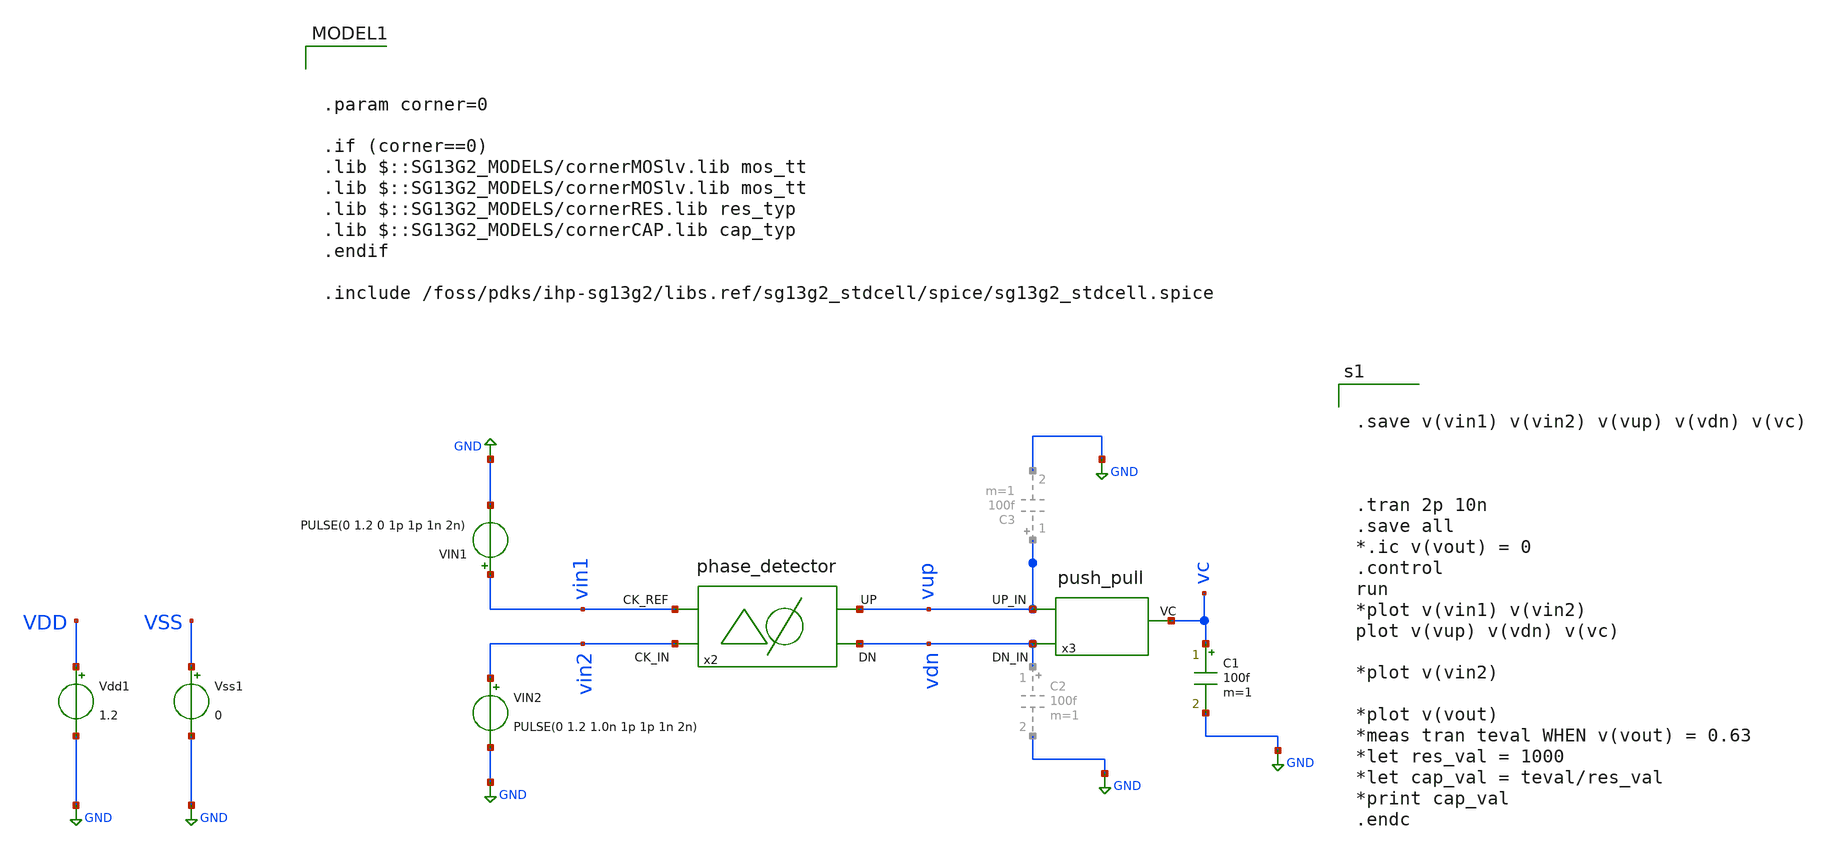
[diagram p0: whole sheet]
** sch_path: xschem/phase_detector/tb_QPD.sch
**.subckt tb_QPD
VIN1 vin1 GND PULSE(0 1.2 0 1p 1p 1n 2n)
x2 vin2 vup vin1 vdn phase_detector
VIN2 vin2 GND PULSE(0 1.2 1.0n 1p 1p 1n 2n)
x3 vup vc vdn push_pull
C1 vc GND 100f m=1
Vss1 VSS GND 0
Vdd1 VDD GND 1.2
**** begin user architecture code


.save v(vin1) v(vin2) v(vup) v(vdn) v(vc)



.tran 2p 10n
.save all
*.ic v(vout) = 0
.control
run
*plot v(vin1) v(vin2)
plot v(vup) v(vdn) v(vc)

*plot v(vin2)

*plot v(vout)
*meas tran teval WHEN v(vout) = 0.63
*let res_val = 1000
*let cap_val = teval/res_val
*print cap_val
.endc




.param corner=0

.if (corner==0)
.lib $::SG13G2_MODELS/cornerMOSlv.lib mos_tt
.lib $::SG13G2_MODELS/cornerMOSlv.lib mos_tt
.lib $::SG13G2_MODELS/cornerRES.lib res_typ
.lib $::SG13G2_MODELS/cornerCAP.lib cap_typ
.endif

.include /foss/pdks/ihp-sg13g2/libs.ref/sg13g2_stdcell/spice/sg13g2_stdcell.spice

**** end user architecture code
**.ends

* expanding   symbol:  /foss/designs/DLL/phase_detector.sym # of pins=4
** sym_path: xschem/phase_detector/phase_detector.sym
** sch_path: xschem/phase_detector/phase_detector.sch
.subckt phase_detector CK_IN UP CK_REF DN
*.opin UP
*.ipin CK_IN
*.ipin CK_REF
*.opin DN
XM7 net2 CK_IN VDD VDD sg13_lv_pmos w=5u l=4u ng=1 m=1 mm_ok=1
XM8 net1 CK_IN VDD VDD sg13_lv_pmos w=5u l=4u ng=1 m=1 mm_ok=1
XM9 net2 CK_REF net1 net1 sg13_lv_nmos w=2u l=5u ng=5 m=1 mm_ok=1
XM10 net2 DN net1 VSS sg13_lv_nmos w=2u l=5u ng=5 m=1 mm_ok=1
XM11 net1 CK_IN VSS VSS sg13_lv_nmos w=2u l=5u ng=5 m=1 mm_ok=1
XM6 UP net2 VDD VDD sg13_lv_pmos w=5u l=4u ng=1 m=1 mm_ok=1
XM12 UP CK_IN net3 net4 sg13_lv_nmos w=2u l=5u ng=5 m=1 mm_ok=1
XM13 net3 net2 net4 net4 sg13_lv_nmos w=2u l=5u ng=5 m=1 mm_ok=1
XM14 net3 net2 VDD VDD sg13_lv_pmos w=5u l=4u ng=1 m=1 mm_ok=1
XM19 net6 CK_IN VDD VDD sg13_lv_pmos w=5u l=4u ng=1 m=1 mm_ok=1
XM20 net5 CK_IN VDD VDD sg13_lv_pmos w=5u l=4u ng=1 m=1 mm_ok=1
XM21 net6 CK_REF net5 net5 sg13_lv_nmos w=2u l=5u ng=5 m=1 mm_ok=1
XM22 net6 UP net5 VSS sg13_lv_nmos w=2u l=5u ng=5 m=1 mm_ok=1
XM23 net5 CK_IN VSS VSS sg13_lv_nmos w=2u l=5u ng=5 m=1 mm_ok=1
XM24 DN net6 VDD VDD sg13_lv_pmos w=5u l=4u ng=1 m=1 mm_ok=1
XM25 DN CK_REF net7 net8 sg13_lv_nmos w=2u l=5u ng=5 m=1 mm_ok=1
XM26 net7 net6 net8 net8 sg13_lv_nmos w=2u l=5u ng=5 m=1 mm_ok=1
XM27 net7 net6 VDD VDD sg13_lv_pmos w=5u l=4u ng=1 m=1 mm_ok=1
.ends


* expanding   symbol:  /foss/designs/DLL/push_pull.sym # of pins=3
** sym_path: xschem/push_pull/push_pull.sym
** sch_path: xschem/push_pull/push_pull.sch
.subckt push_pull UP_IN VC DN_IN
*.opin VC
*.ipin UP_IN
*.ipin DN_IN
XM1 net1 DN_IN net2 VSS sg13_lv_nmos w=0.3u l=0.45u ng=1 m=1 mm_ok=1
XM7 net1 net1 VDD VDD sg13_lv_pmos w=0.15u l=0.13u ng=1 m=1 mm_ok=1
XM2 net7 DNB net2 VSS sg13_lv_nmos w=0.3u l=0.45u ng=1 m=1 mm_ok=1
XM3 net2 VDD VSS VSS sg13_lv_nmos w=0.3u l=0.45u ng=1 m=1 mm_ok=1
XM4 net1 net1 VDD VDD sg13_lv_pmos w=0.15u l=0.13u ng=1 m=1 mm_ok=1
XM5 net5 net7 VDD VDD sg13_lv_pmos w=0.15u l=0.13u ng=1 m=1 mm_ok=1
XM6 net4 UPB net3 VSS sg13_lv_nmos w=0.3u l=0.45u ng=1 m=1 mm_ok=1
XM8 net6 net4 VDD VDD sg13_lv_pmos w=0.15u l=0.13u ng=1 m=1 mm_ok=1
XM9 VC UP_IN net3 VSS sg13_lv_nmos w=0.3u l=0.45u ng=1 m=1 mm_ok=1
XM10 net3 VDD VSS VSS sg13_lv_nmos w=0.3u l=0.45u ng=1 m=1 mm_ok=1
XM11 VC net1 VDD VDD sg13_lv_pmos w=0.15u l=0.13u ng=1 m=1 mm_ok=1
XM12 VC net1 VDD VDD sg13_lv_pmos w=0.15u l=0.13u ng=1 m=1 mm_ok=1
XM13 net6 net4 VDD VDD sg13_lv_pmos w=0.15u l=0.13u ng=1 m=1 mm_ok=1
XM14 net5 net7 VDD VDD sg13_lv_pmos w=0.15u l=0.13u ng=1 m=1 mm_ok=1
x1 VDD DN_IN DNB VSS inv_1_manual
x2 VDD UP_IN UPB VSS inv_1_manual
.ends


* expanding   symbol:  /foss/designs/UNIC-CASS-Aug25/sch/inv_1_manual/inv_1_manual.sym # of pins=4
** sym_path: xschem/inv_1_manual/inv_1_manual.sym
** sch_path: xschem/inv_1_manual/inv_1_manual.sch
.subckt inv_1_manual VDD_D A Y VSS_D
*.iopin VDD_D
*.iopin VSS_D
*.iopin A
*.iopin Y
XM1 Y A VSS_D VSS_D sg13_lv_nmos w=10u l=0.13u ng=1 m=1 mm_ok=1
XM2 Y A VDD_D VDD_D sg13_lv_pmos w=10u l=0.13u ng=1 m=1 mm_ok=1
.ends

.GLOBAL GND
.end
